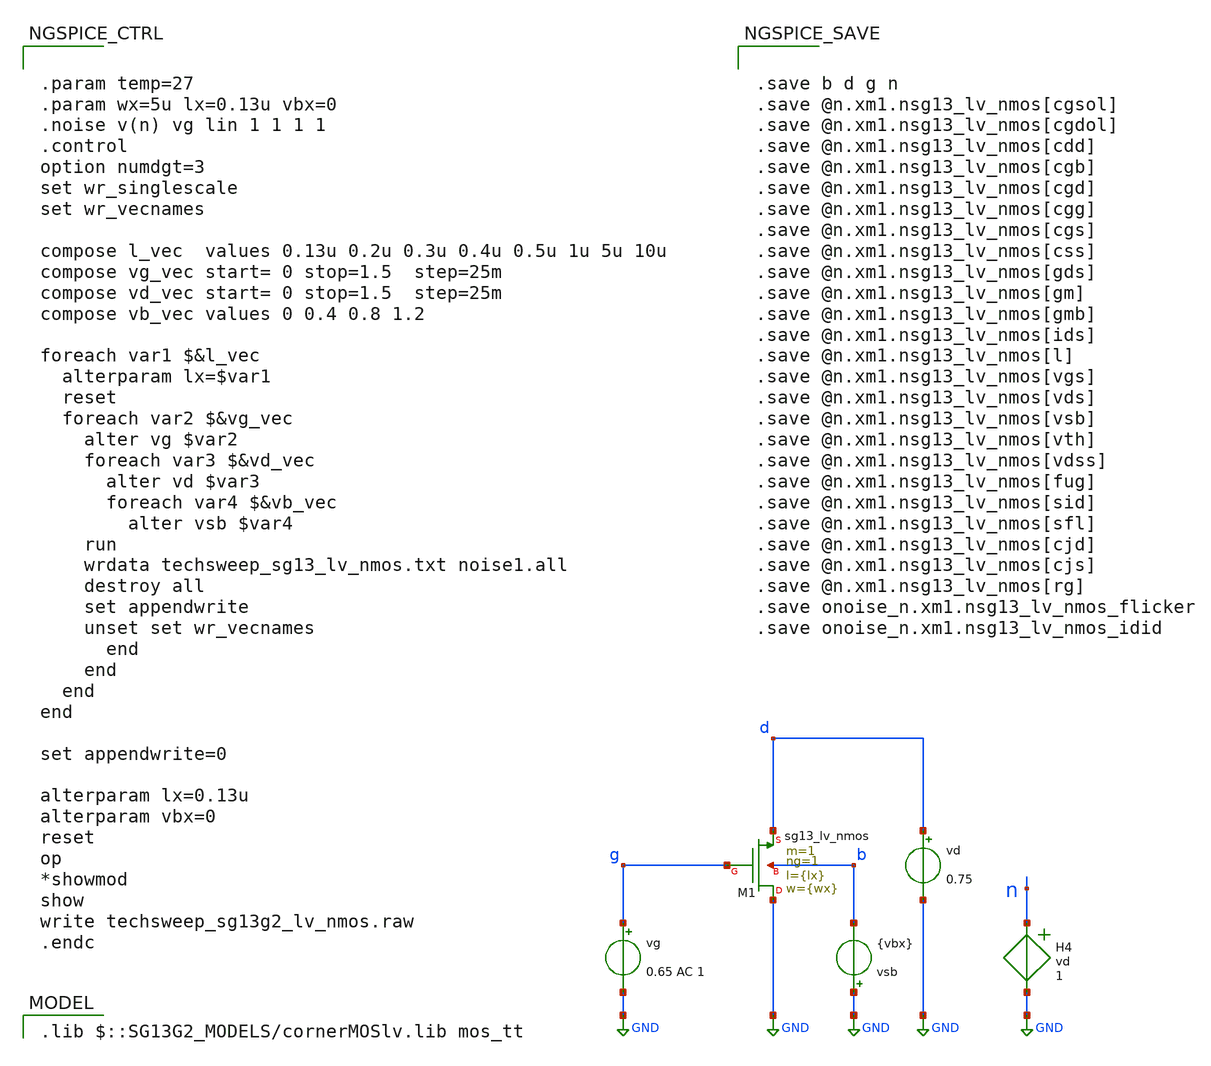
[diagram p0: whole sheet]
** sch_path: xschem/techsweep_sg13g2_lv_nmos.sch
* (c) 2024 Harald Pretl (adapted from Boris Murmann)
**.subckt techsweep_sg13g2_lv_nmos
vg g GND 0.65 AC 1
vd d GND 0.75
XM1 GND g d b sg13_lv_nmos w={wx} l={lx} ng=1 m=1 mm_ok=1
vsb GND b {vbx}
H4 n GND vd 1
**** begin user architecture code
 .lib $::SG13G2_MODELS/cornerMOSlv.lib mos_tt



.param temp=27
.param wx=5u lx=0.13u vbx=0
.noise v(n) vg lin 1 1 1 1
.control
option numdgt=3
set wr_singlescale
set wr_vecnames

compose l_vec  values 0.13u 0.2u 0.3u 0.4u 0.5u 1u 5u 10u
compose vg_vec start= 0 stop=1.5  step=25m
compose vd_vec start= 0 stop=1.5  step=25m
compose vb_vec values 0 0.4 0.8 1.2

foreach var1 $&l_vec
  alterparam lx=$var1
  reset
  foreach var2 $&vg_vec
    alter vg $var2
    foreach var3 $&vd_vec
      alter vd $var3
      foreach var4 $&vb_vec
        alter vsb $var4
	run
	wrdata techsweep_sg13_lv_nmos.txt noise1.all
	destroy all
	set appendwrite
	unset set wr_vecnames
      end
    end
  end
end

set appendwrite=0

alterparam lx=0.13u
alterparam vbx=0
reset
op
*showmod
show
write techsweep_sg13g2_lv_nmos.raw
.endc




.save b d g n
.save @n.xm1.nsg13_lv_nmos[cgsol]
.save @n.xm1.nsg13_lv_nmos[cgdol]
.save @n.xm1.nsg13_lv_nmos[cdd]
.save @n.xm1.nsg13_lv_nmos[cgb]
.save @n.xm1.nsg13_lv_nmos[cgd]
.save @n.xm1.nsg13_lv_nmos[cgg]
.save @n.xm1.nsg13_lv_nmos[cgs]
.save @n.xm1.nsg13_lv_nmos[css]
.save @n.xm1.nsg13_lv_nmos[gds]
.save @n.xm1.nsg13_lv_nmos[gm]
.save @n.xm1.nsg13_lv_nmos[gmb]
.save @n.xm1.nsg13_lv_nmos[ids]
.save @n.xm1.nsg13_lv_nmos[l]
.save @n.xm1.nsg13_lv_nmos[vgs]
.save @n.xm1.nsg13_lv_nmos[vds]
.save @n.xm1.nsg13_lv_nmos[vsb]
.save @n.xm1.nsg13_lv_nmos[vth]
.save @n.xm1.nsg13_lv_nmos[vdss]
.save @n.xm1.nsg13_lv_nmos[fug]
.save @n.xm1.nsg13_lv_nmos[sid]
.save @n.xm1.nsg13_lv_nmos[sfl]
.save @n.xm1.nsg13_lv_nmos[cjd]
.save @n.xm1.nsg13_lv_nmos[cjs]
.save @n.xm1.nsg13_lv_nmos[rg]
.save onoise_n.xm1.nsg13_lv_nmos_flicker
.save onoise_n.xm1.nsg13_lv_nmos_idid


**** end user architecture code
**.ends
.GLOBAL GND
.end
